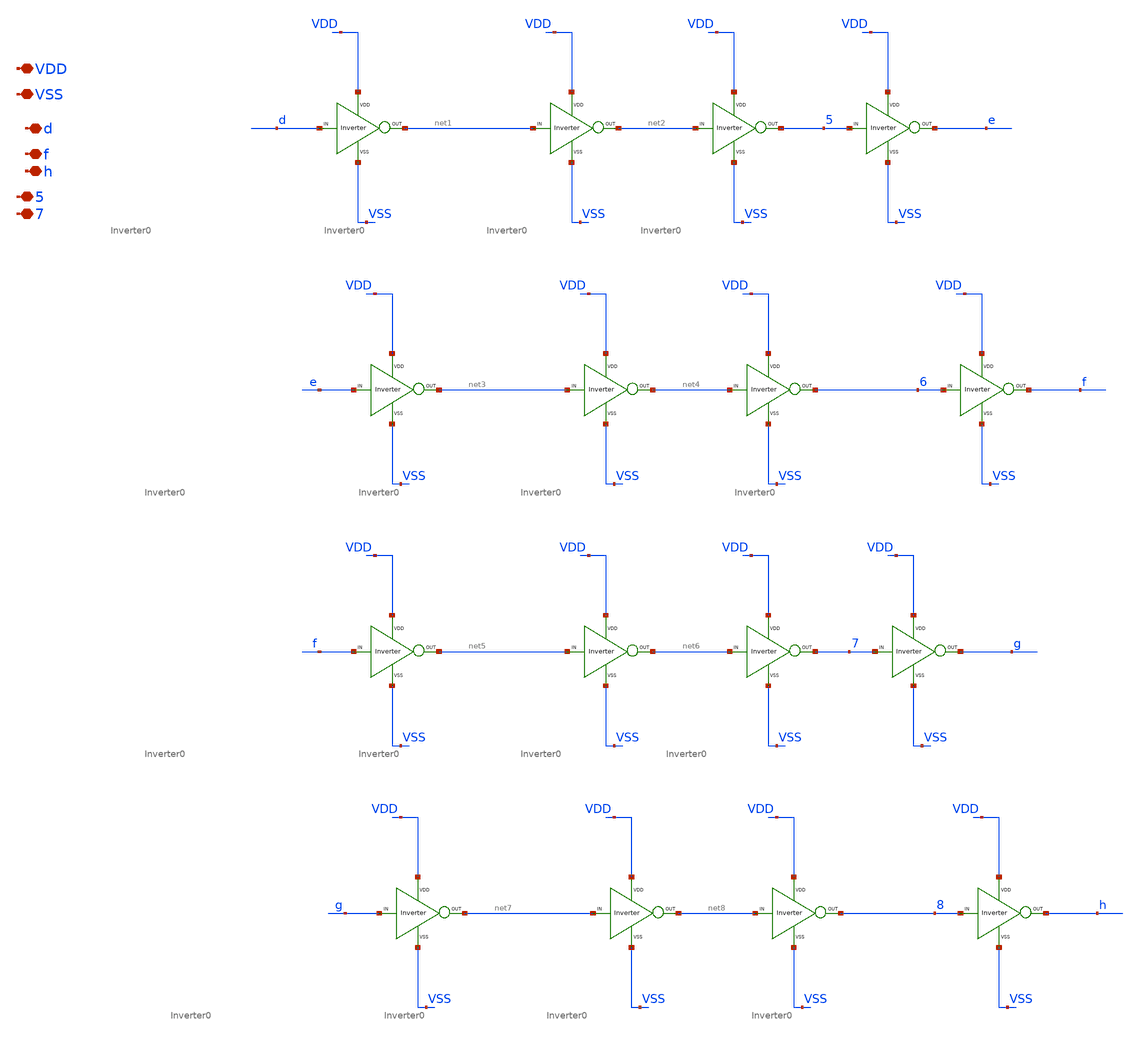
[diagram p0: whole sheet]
** sch_path: xschem/DC_DC_Converter_xschem/DC_DC_Converter/Delay_block_revised/delay2.sch
**.subckt delay2 VDD VSS d h 5 7 f
*.iopin VDD
*.iopin VSS
*.iopin d
*.iopin h
*.iopin 5
*.iopin 7
*.iopin f
X12 d net1 VDD VSS Inverter0
X14 net1 net2 VDD VSS Inverter0
X15 5 e VDD VSS Inverter0
X16 e net3 VDD VSS Inverter0
X17 net3 net4 VDD VSS Inverter0
X18 6 f VDD VSS Inverter0
X19 f net5 VDD VSS Inverter0
X20 net5 net6 VDD VSS Inverter0
X21 7 g VDD VSS Inverter0
X22 g net7 VDD VSS Inverter0
X23 net7 net8 VDD VSS Inverter0
X24 8 h VDD VSS Inverter0
X29 net2 5 VDD VSS Inverter0
X30 net4 6 VDD VSS Inverter0
X31 net6 7 VDD VSS Inverter0
X32 net8 8 VDD VSS Inverter0
**.ends

* expanding   symbol:  DC_DC_Converter/Delay_block_revised/Inverter_0/Inverter0.sym # of pins=4
** sym_path: xschem/DC_DC_Converter_xschem/DC_DC_Converter/Delay_block_revised/Inverter_0/Inverter0.sym
** sch_path: xschem/DC_DC_Converter_xschem/DC_DC_Converter/Delay_block_revised/Inverter_0/Inverter0.sch
.subckt Inverter0 VIN VOUT VDD VSS
*.ipin VIN
*.iopin VDD
*.iopin VSS
*.opin VOUT
XM1 VOUT VIN VSS VSS sky130_fd_pr__nfet_01v8 L=0.15 W=0.4 nf=1 ad='int((nf+1)/2) * W/nf * 0.29' as='int((nf+2)/2) * W/nf * 0.29'
+ pd='2*int((nf+1)/2) * (W/nf + 0.29)' ps='2*int((nf+2)/2) * (W/nf + 0.29)' nrd='0.29 / W' nrs='0.29 / W'
+ sa=0 sb=0 sd=0 mult=1 m=1
XM2 VOUT VIN VDD VDD sky130_fd_pr__pfet_01v8 L=0.15 W=1.2 nf=1 ad='int((nf+1)/2) * W/nf * 0.29' as='int((nf+2)/2) * W/nf * 0.29'
+ pd='2*int((nf+1)/2) * (W/nf + 0.29)' ps='2*int((nf+2)/2) * (W/nf + 0.29)' nrd='0.29 / W' nrs='0.29 / W'
+ sa=0 sb=0 sd=0 mult=1 m=1
.ends

.end
